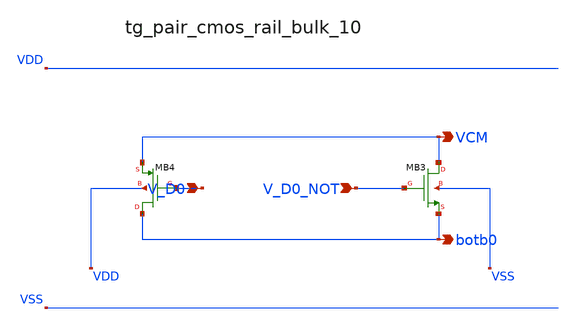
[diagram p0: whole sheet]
** sch_path: analog-db/raw/ia_005_hsu_pga_ideal/hier/blocks/tg_pair_cmos_rail_bulk_10.sch
**.subckt tg_pair_cmos_rail_bulk_10 V_D0 V_D0_NOT VCM botb0
*.ipin V_D0
*.ipin V_D0_NOT
*.opin VCM
*.opin botb0
XMB3 VCM V_D0_NOT botb0 VSS sg13_lv_nmos w=x_dut_xmb3_w l=x_dut_xmb3_l ng=1 m=x_dut_xmb3_m
XMB4 botb0 V_D0 VCM VDD sg13_lv_pmos w=x_dut_xmb4_w l=x_dut_xmb4_l ng=1 m=x_dut_xmb4_m
**.ends
.end
